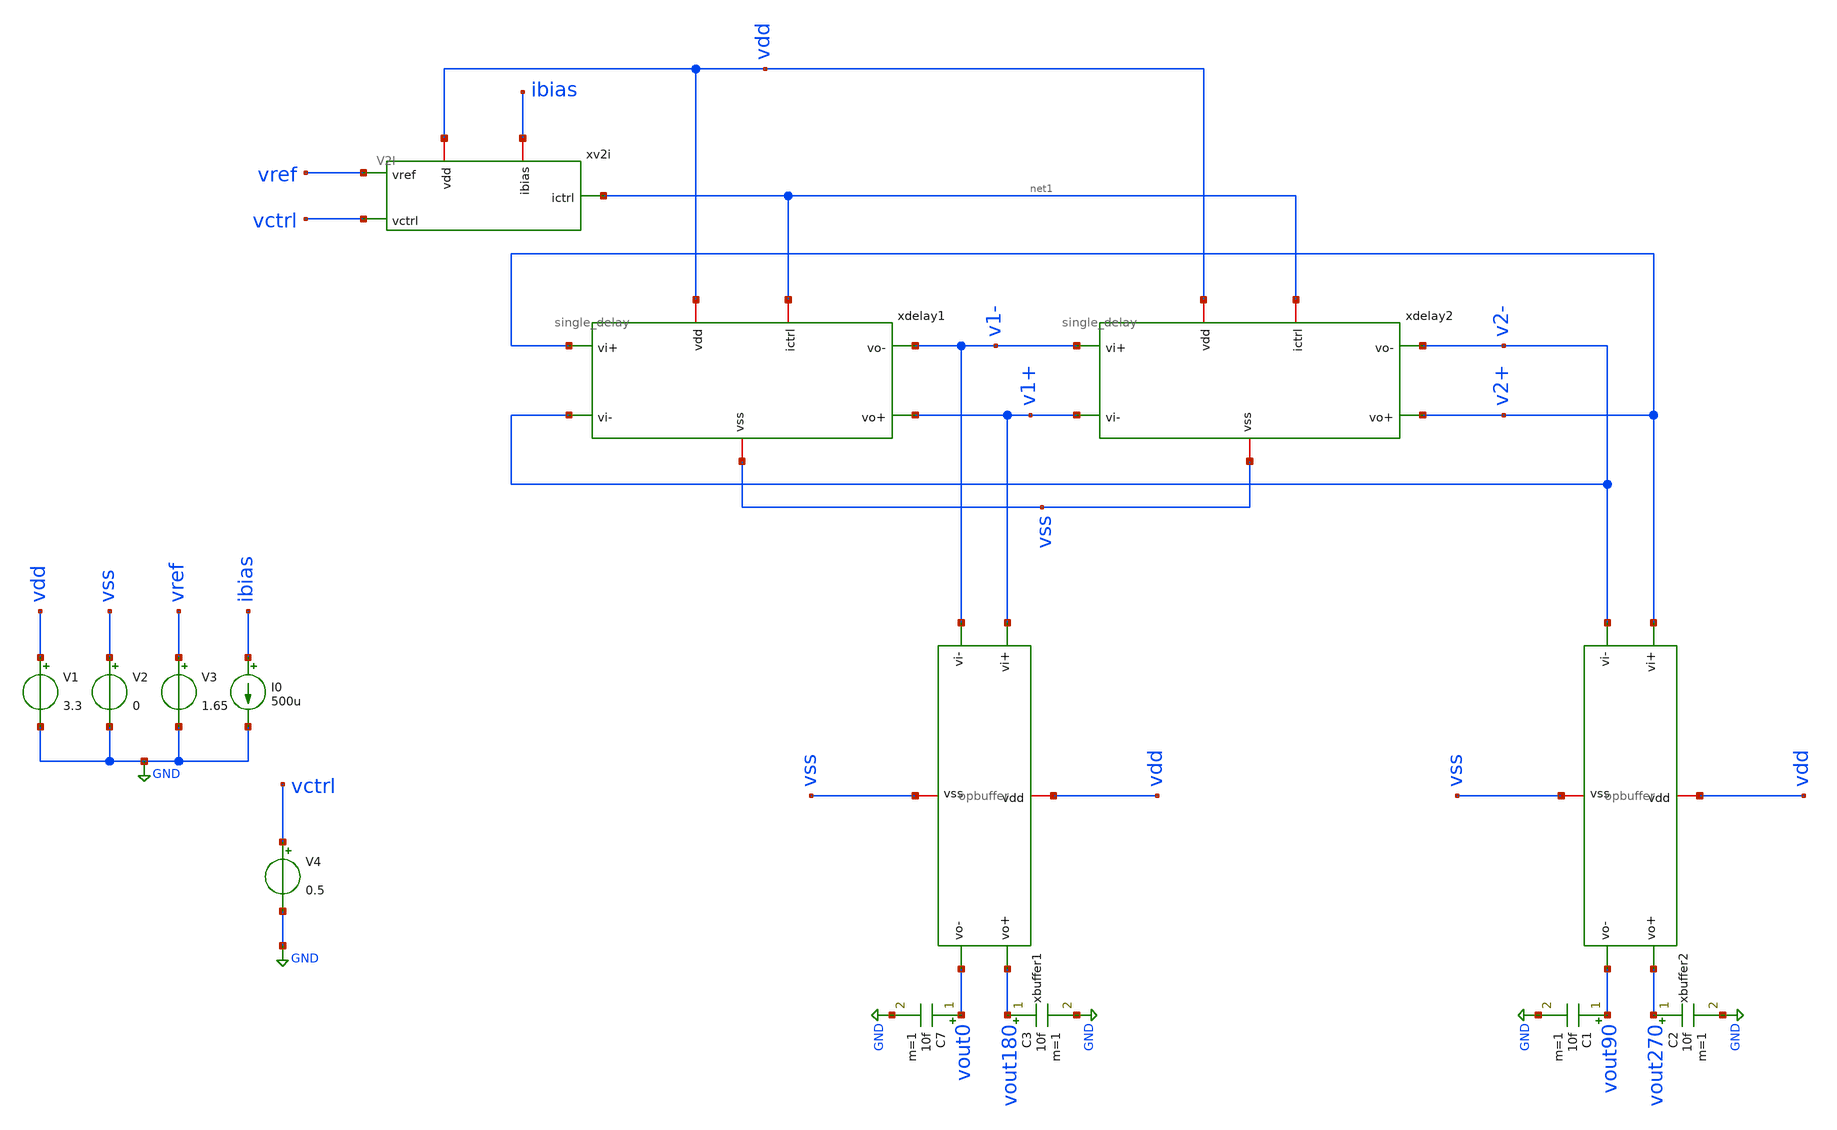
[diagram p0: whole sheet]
** sch_path: xschem/power_tb.sch
**.subckt power_tb
xdelay1 net1 vdd v2+ v2- v1- v1+ vss single_delay
xdelay2 net1 vdd v1- v1+ v2- v2+ vss single_delay
xv2i vdd net1 vref vctrl ibias V2I
xbuffer2 vdd vss v2+ vout270 vout90 v2- opbuffer
V1 vdd GND 3.3
V2 vss GND 0
V3 vref GND 1.65
I0 ibias GND 500u
V4 vctrl GND 0.5
xbuffer1 vdd vss v1+ vout180 vout0 v1- opbuffer
C7 vout0 GND 10f m=1
C1 vout90 GND 10f m=1
C2 vout270 GND 10f m=1
C3 vout180 GND 10f m=1
**** begin user architecture code


.control
let start_v = 0.5
let stop_v  = 3.3
let step_v  = 0.05

let vctrl = start_v

let v_sweep = unitvec(57)
let power_results = unitvec(57)
let i = 0

dowhile vctrl <= stop_v
	alter @V4[DC] = vctrl
	tran 10p 50n
	meas tran irms RMS v(v1#branch) from=40n to=50n
	let power_rms = irms * 3.3
	let v_sweep[i] = $&vctrl
	let power_results[i] = power_rms
	print power_rms
	let vctrl = vctrl + step_v
	let i = i + 1
	reset
end
set nolegend
print power_results
set filetype=ascii
write /foss/designs/vco_des/xschem/power.txt power_results
.endc



.include $::180MCU_MODELS/design.ngspice
.lib $::180MCU_MODELS/sm141064.ngspice typical
.lib $::180MCU_MODELS/sm141064.ngspice cap_mim
.lib $::180MCU_MODELS/sm141064.ngspice res_typical
.lib $::180MCU_MODELS/sm141064.ngspice mimcap_typical

**** end user architecture code
**.ends
.GLOBAL GND
.end
